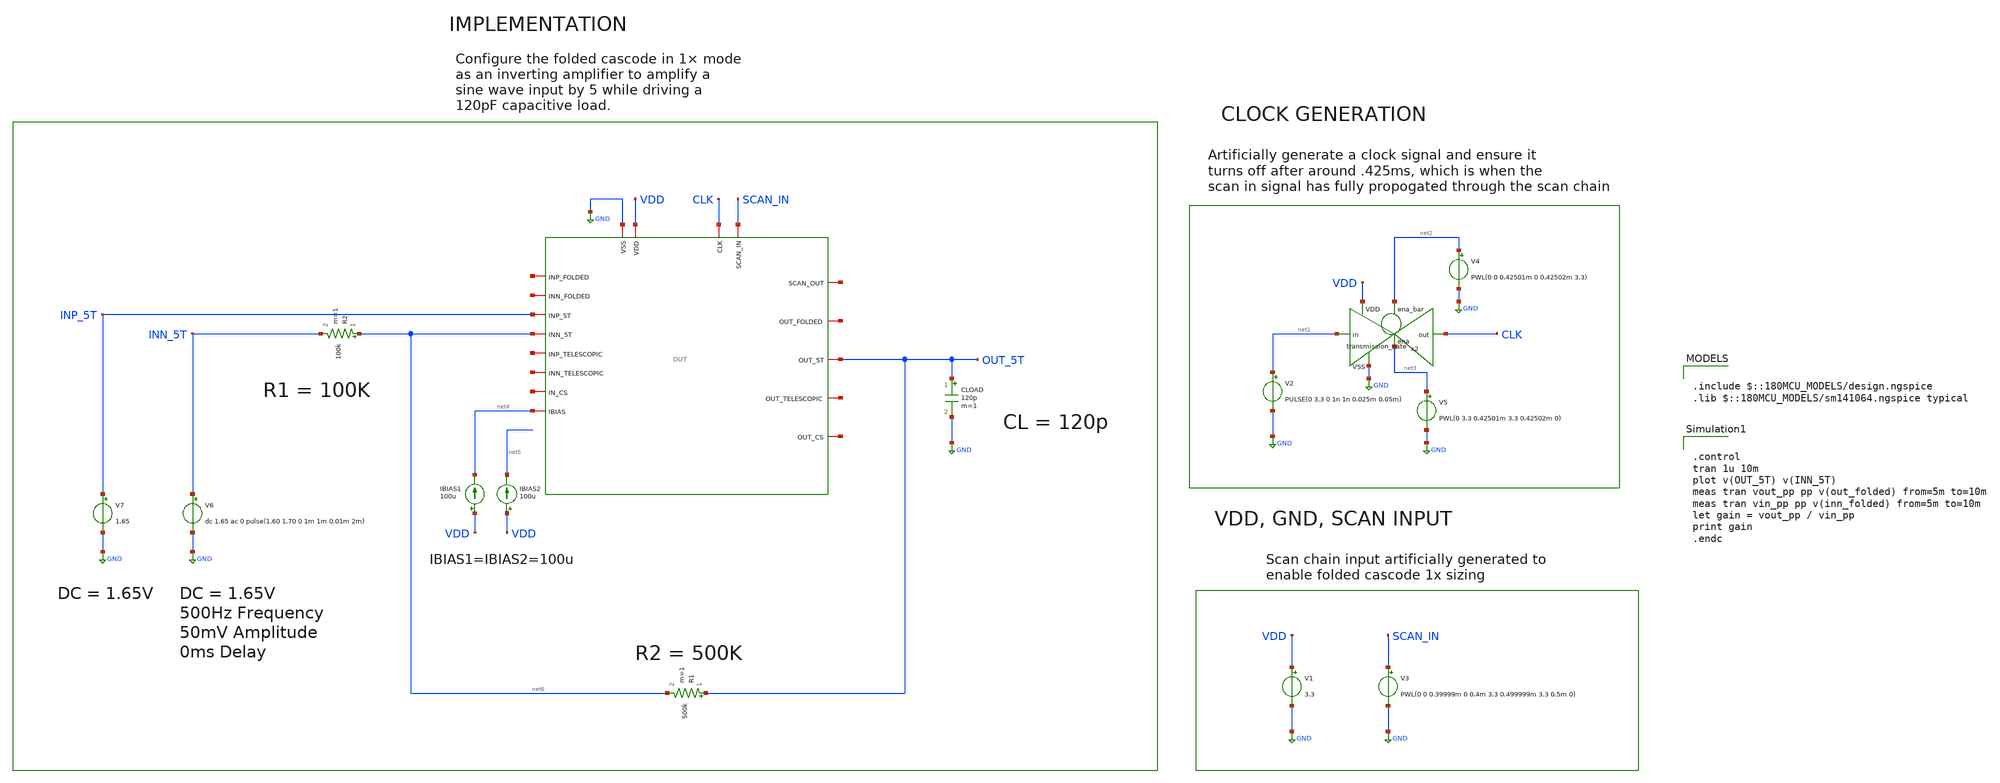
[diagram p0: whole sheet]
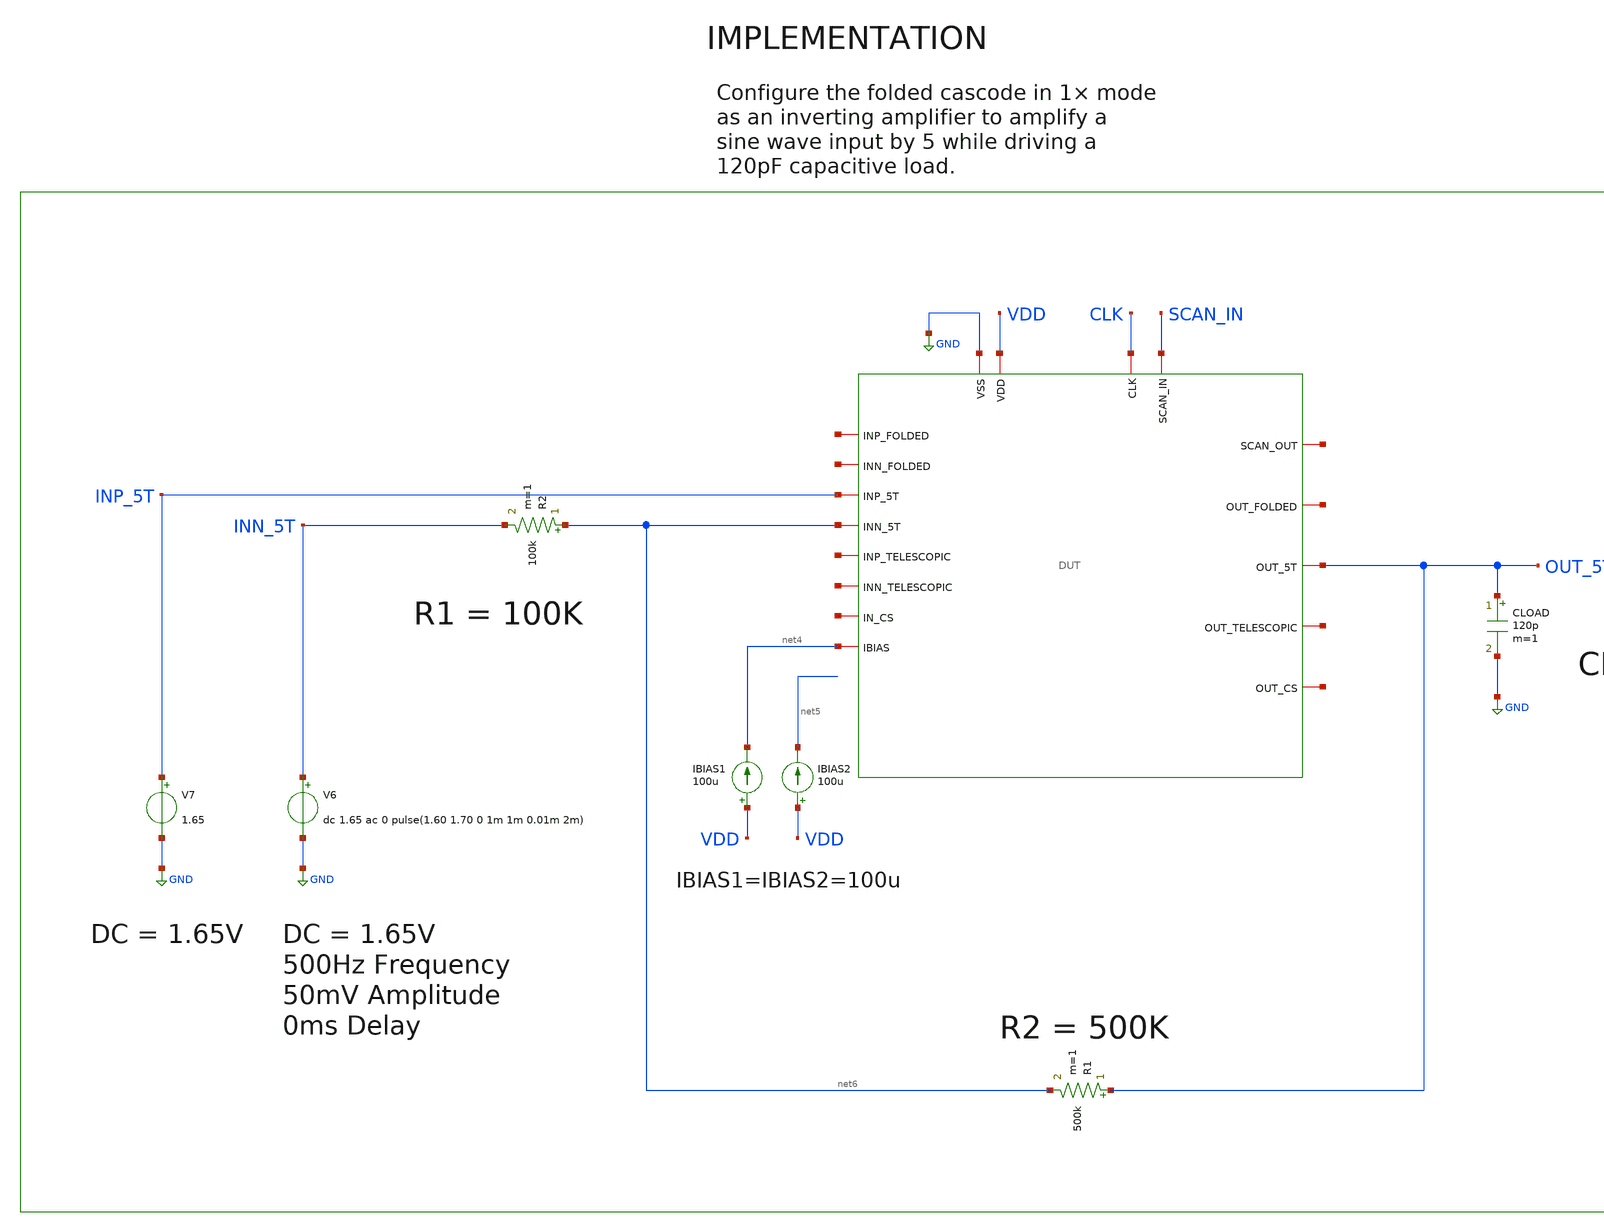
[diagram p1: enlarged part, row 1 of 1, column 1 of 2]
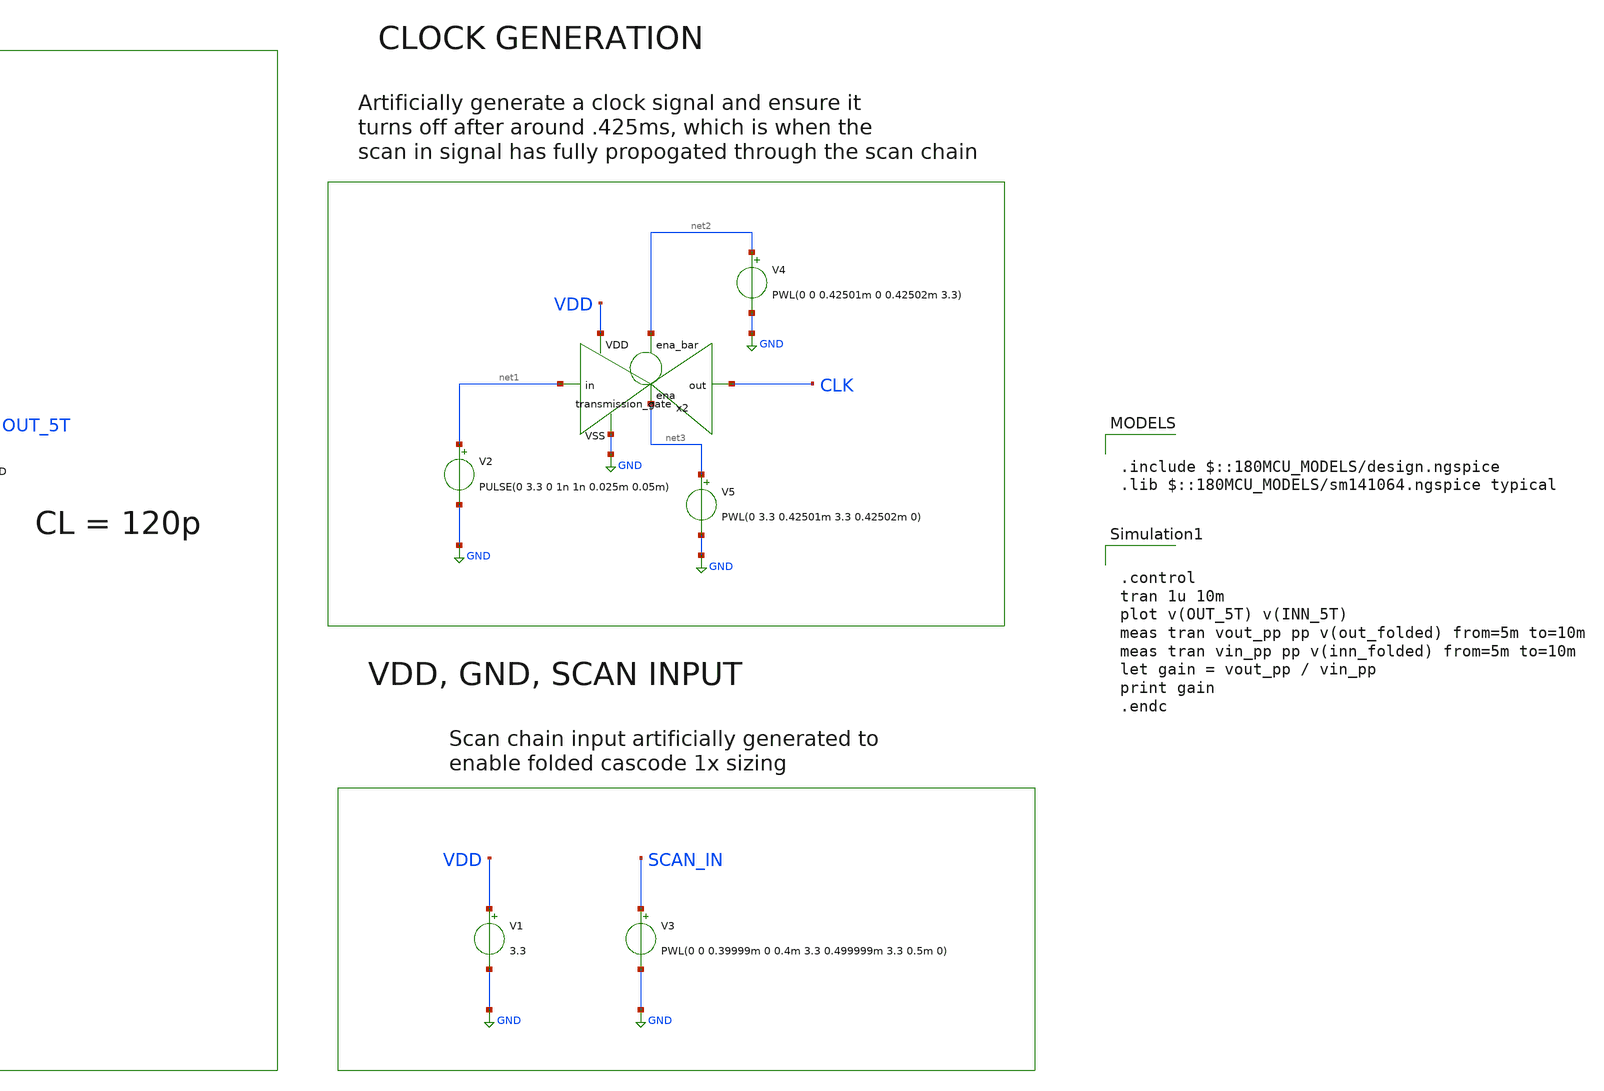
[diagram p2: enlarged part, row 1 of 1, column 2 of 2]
** sch_path: designs/libs/core_tb/etj/ota_5t/5t_input_triangle_1x.sch
**.subckt 5t_input_triangle_1x
V3 SCAN_IN GND PWL(0 0 0.39999m 0 0.4m 3.3 0.499999m 3.3 0.5m 0)
V1 VDD GND 3.3
V2 net1 GND PULSE(0 3.3 0 1n 1n 0.025m 0.05m)
x2 net2 VDD CLK net1 GND net3 transmission_gate
V4 net2 GND PWL(0 0 0.42501m 0 0.42502m 3.3)
V5 net3 GND PWL(0 3.3 0.42501m 3.3 0.42502m 0)
IBIAS1 VDD net4 100u
IBIAS2 VDD net5 100u
V7 INP_5T GND 1.65
CLOAD OUT_5T GND 120p m=1
R2 net6 INN_5T 100k m=1
V6 INN_5T GND dc 1.65 ac 0 pulse(1.60 1.70 0 1m 1m 0.01m 2m)
R1 OUT_5T net6 500k m=1
x1 CLK net7 SCAN_IN GND VDD net8 net9 OUT_5T net4 net10 INP_5T net6 net11 net12 net13 net14 net15
+ DUT
**** begin user architecture code

.include $::180MCU_MODELS/design.ngspice
.lib $::180MCU_MODELS/sm141064.ngspice typical



.control
tran 1u 10m
plot v(OUT_5T) v(INN_5T)
meas tran vout_pp pp v(out_folded) from=5m to=10m
meas tran vin_pp pp v(inn_folded) from=5m to=10m
let gain = vout_pp / vin_pp
print gain
.endc


**** end user architecture code
**.ends
.GLOBAL GND
.end
